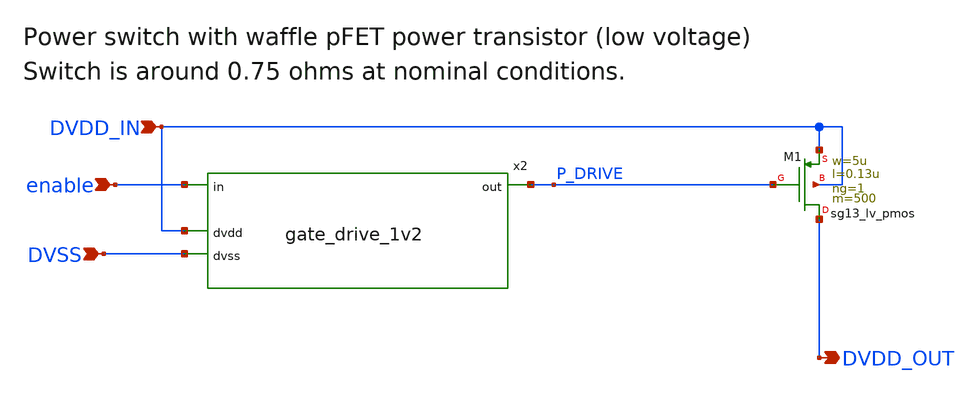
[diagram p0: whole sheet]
** sch_path: xschem/power_stage1v2.sch
**.subckt power_stage1v2 enable DVDD_IN DVSS DVDD_OUT
*.ipin enable
*.ipin DVDD_IN
*.ipin DVSS
*.opin DVDD_OUT
x2 enable P_DRIVE DVDD_IN DVSS gate_drive_1v2
XM1 DVDD_OUT P_DRIVE DVDD_IN DVDD_IN sg13_lv_pmos w=5u l=0.13u ng=1 m=500 mm_ok=1
**.ends

* expanding   symbol:  gate_drive_1v2.sym # of pins=4
** sym_path: xschem/gate_drive_1v2.sym
** sch_path: xschem/gate_drive_1v2.sch
.subckt gate_drive_1v2 in out dvdd dvss
*.opin out
*.ipin in
*.iopin dvdd
*.iopin dvss
x2 net1 net3 dvdd dvss sg13cmos5l_inv_2
x3 net2 net1 dvdd dvss sg13cmos5l_inv_8
x4 net4 net2 dvdd dvss sg13cmos5l_inv_16
x6 net3 in dvdd dvss sg13cmos5l_inv_1
x7 in dvdd dvss sg13cmos5l_antennanp
x8[1] dvdd dvss sg13cmos5l_decap_4
x8[0] dvdd dvss sg13cmos5l_decap_4
XM1 out net4 dvss dvss sg13_lv_nmos w=26.64u l=0.13u ng=36 m=1 mm_ok=1
XM2 out net4 dvdd dvdd sg13_lv_pmos w=40.32u l=0.13u ng=36 m=1 mm_ok=1
.ends

.end
